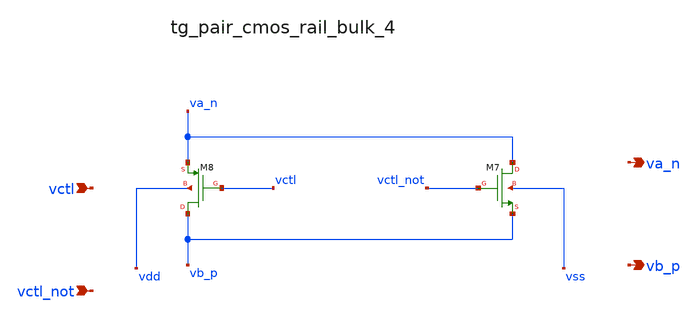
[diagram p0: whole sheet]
** sch_path: analog-db/raw/sw_002_chopper_diff/hier/blocks/tg_pair_cmos_rail_bulk_4.sch
**.subckt tg_pair_cmos_rail_bulk_4 vctl vctl_not va_n vb_p
*.ipin vctl
*.ipin vctl_not
*.opin va_n
*.opin vb_p
XM7 va_n vctl_not vb_p vss sg13_lv_nmos w=x_dut_xm7_w l=x_dut_xm7_l ng=1 m=x_dut_xm7_m
XM8 vb_p vctl va_n vdd sg13_lv_pmos w=x_dut_xm8_w l=x_dut_xm8_l ng=1 m=x_dut_xm8_m
**.ends
.end
